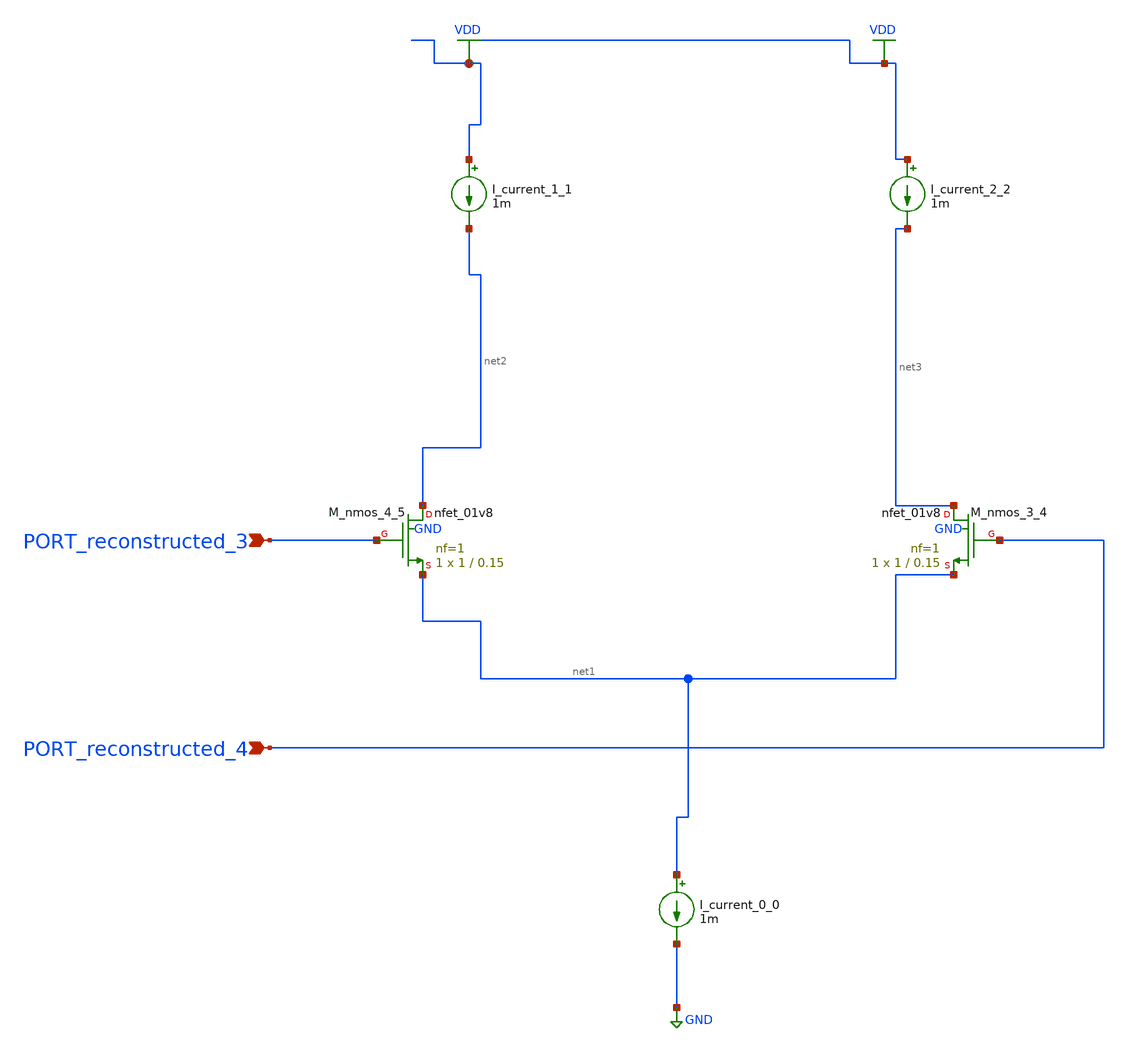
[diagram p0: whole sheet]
** sch_path: schematics/AMSNet/752.sch
**.subckt 752 PORT_reconstructed_4 PORT_reconstructed_3
*.ipin PORT_reconstructed_4
*.ipin PORT_reconstructed_3
I_current_0_0 net1 GND 1m
I_current_1_1 VDD net2 1m
I_current_2_2 VDD net3 1m
XM_nmos_3_4 net3 PORT_reconstructed_4 net1 GND sky130_fd_pr__nfet_01v8 L=0.15 W=1 nf=1 ad='int((1 + 1)/2) * 1 / 1 * 0.29'
+ as='int((1 + 2)/2) * 1 / 1 * 0.29' pd='2*int((1 + 1)/2) * (1 / 1 + 0.29)' ps='2*int((1 + 2)/2) * (1 / 1 + 0.29)'
+ nrd='0.29 / 1 ' nrs='0.29 / 1 ' sa=0 sb=0 sd=0 mult=1 m=1
XM_nmos_4_5 net2 PORT_reconstructed_3 net1 GND sky130_fd_pr__nfet_01v8 L=0.15 W=1 nf=1 ad='int((1 + 1)/2) * 1 / 1 * 0.29'
+ as='int((1 + 2)/2) * 1 / 1 * 0.29' pd='2*int((1 + 1)/2) * (1 / 1 + 0.29)' ps='2*int((1 + 2)/2) * (1 / 1 + 0.29)'
+ nrd='0.29 / 1 ' nrs='0.29 / 1 ' sa=0 sb=0 sd=0 mult=1 m=1
**.ends
.GLOBAL GND
.GLOBAL VDD
.end
